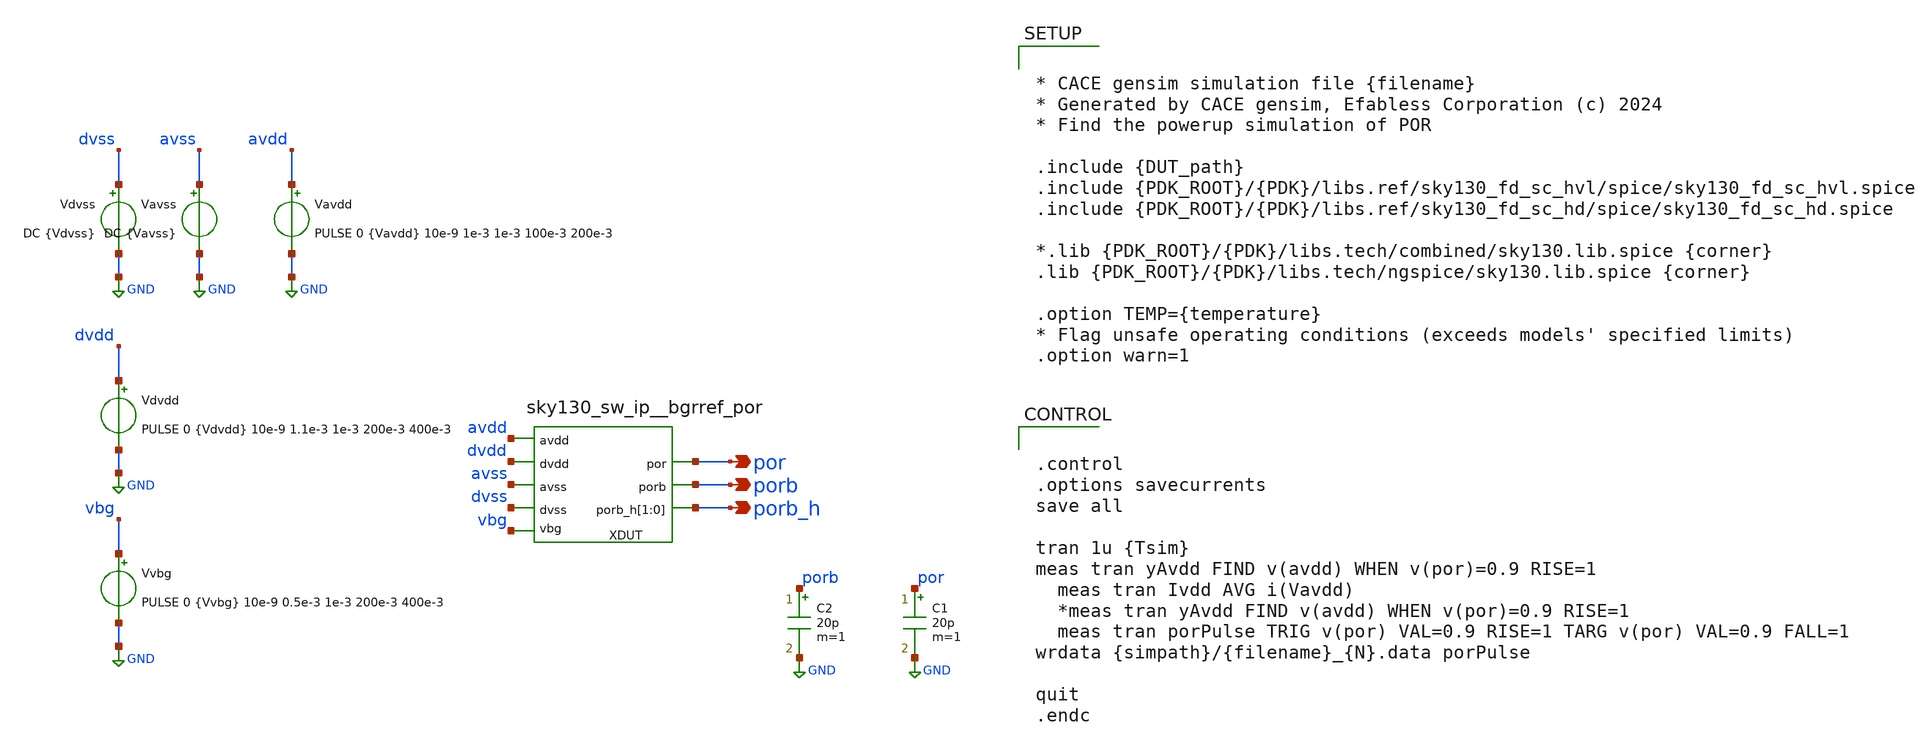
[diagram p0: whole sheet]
** sch_path: cace/templates/orig/por_sim.sch
**.subckt por_sim por porb porb_h
*.opin por
*.opin porb
*.opin porb_h
Vdvss dvss GND DC {Vdvss}
Vavdd avdd GND PULSE 0 {Vavdd} 10e-9 1e-3 1e-3 100e-3 200e-3
Vavss avss GND DC {Vavss}
Vdvdd dvdd GND PULSE 0 {Vdvdd} 10e-9 1.1e-3 1e-3 200e-3 400e-3
Vvbg vbg GND PULSE 0 {Vvbg} 10e-9 0.5e-3 1e-3 200e-3 400e-3
XDUT vbg por avss avdd dvdd porb dvss porb_h porb_h sky130_sw_ip__bgrref_por
C1 por GND 20p m=1
C2 porb GND 20p m=1
**** begin user architecture code


* CACE gensim simulation file {filename}
* Generated by CACE gensim, Efabless Corporation (c) 2024
* Find the powerup simulation of POR

.include {DUT_path}
.include {PDK_ROOT}/{PDK}/libs.ref/sky130_fd_sc_hvl/spice/sky130_fd_sc_hvl.spice
.include {PDK_ROOT}/{PDK}/libs.ref/sky130_fd_sc_hd/spice/sky130_fd_sc_hd.spice

*.lib {PDK_ROOT}/{PDK}/libs.tech/combined/sky130.lib.spice {corner}
.lib {PDK_ROOT}/{PDK}/libs.tech/ngspice/sky130.lib.spice {corner}

.option TEMP={temperature}
* Flag unsafe operating conditions (exceeds models' specified limits)
.option warn=1




.control
.options savecurrents
save all

tran 1u {Tsim}
meas tran yAvdd FIND v(avdd) WHEN v(por)=0.9 RISE=1
  meas tran Ivdd AVG i(Vavdd)
  *meas tran yAvdd FIND v(avdd) WHEN v(por)=0.9 RISE=1
  meas tran porPulse TRIG v(por) VAL=0.9 RISE=1 TARG v(por) VAL=0.9 FALL=1
wrdata {simpath}/{filename}_{N}.data porPulse

quit
.endc


**** end user architecture code
**.ends
.GLOBAL GND
.end
